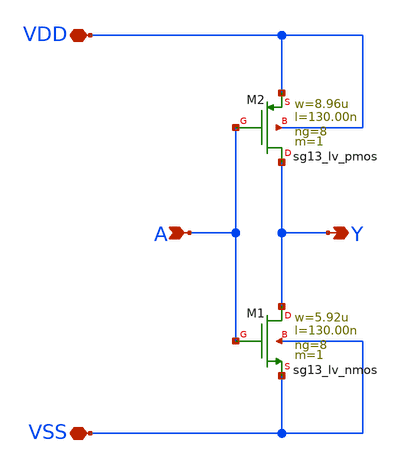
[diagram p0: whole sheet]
** sch_path: ihp-sg13g2/libs.tech/xschem/sg13g2_stdcells/sg13g2_inv_8.sch
* Copyright 2023 IHP PDK Authors
* Licensed under the Apache License, Version 2.0 (the "License");
* you may not use this file except in compliance with the License.
* You may obtain a copy of the License at
* https://www.apache.org/licenses/LICENSE-2.0
* Unless required by applicable law or agreed to in writing, software
* distributed under the License is distributed on an "AS IS" BASIS,
* WITHOUT WARRANTIES OR CONDITIONS OF ANY KIND, either express or implied.
* See the License for the specific language governing permissions and
* limitations under the License.
**.subckt sg13g2_inv_8 Y A VDD VSS
*.opin Y
*.ipin A
*.iopin VDD
*.iopin VSS
XM1 Y A VSS VSS sg13_lv_nmos w=5.92u l=130.00n ng=8 m=1 mm_ok=1
XM2 Y A VDD VDD sg13_lv_pmos w=8.96u l=130.00n ng=8 m=1 mm_ok=1
**.ends
.end
